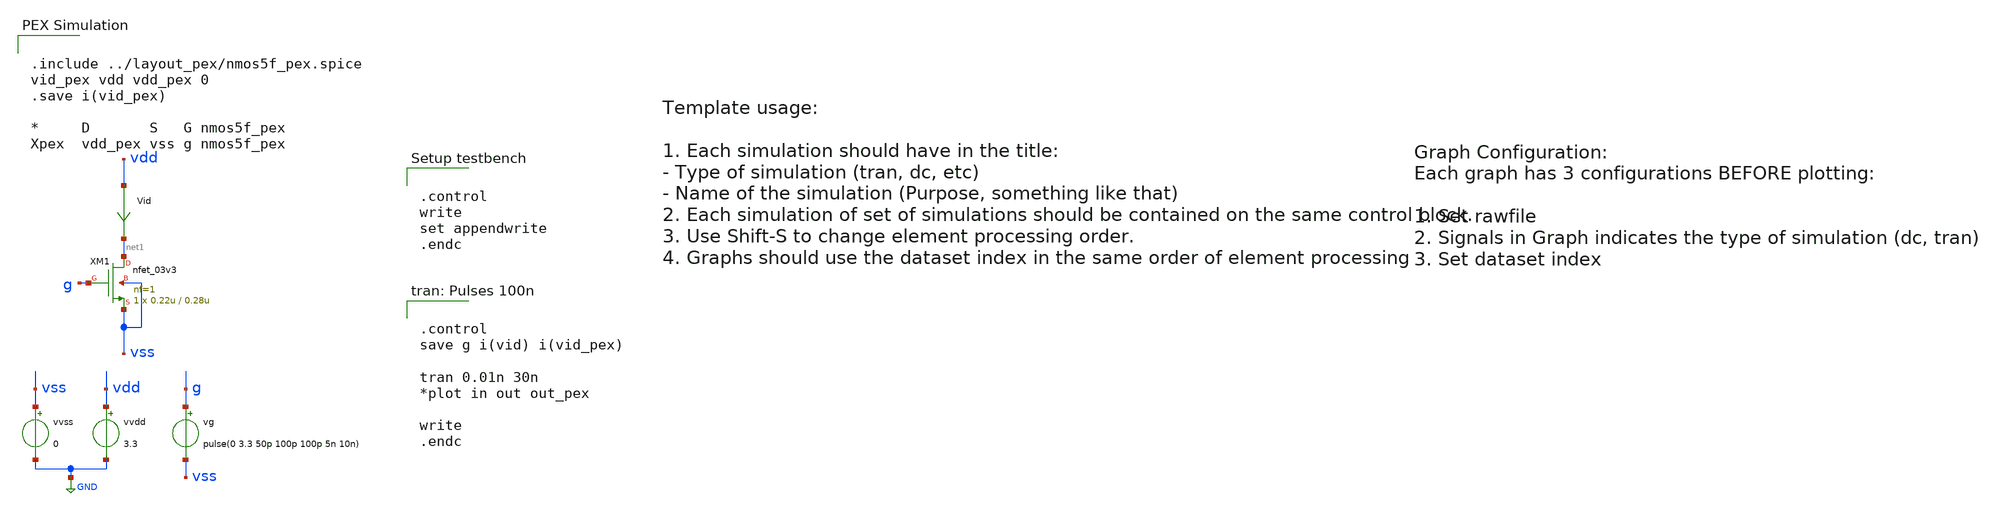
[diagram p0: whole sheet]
** sch_path: samples/gf180mcu/nmos5f/test/nmos5f.sch

.include $env(PDK_ROOT)/$env(PDK)/libs.tech/ngspice/design.ngspice
.lib $env(PDK_ROOT)/$env(PDK)/libs.tech/ngspice/sm141064.ngspice typical
.lib $env(PDK_ROOT)/$env(PDK)/libs.tech/ngspice/sm141064.ngspice mimcap_statistical
.lib $env(PDK_ROOT)/$env(PDK)/libs.tech/ngspice/sm141064.ngspice cap_mim
.lib $env(PDK_ROOT)/$env(PDK)/libs.tech/ngspice/sm141064.ngspice res_typical
.lib $env(PDK_ROOT)/$env(PDK)/libs.tech/ngspice/sm141064.ngspice bjt_typical
.lib $env(PDK_ROOT)/$env(PDK)/libs.tech/ngspice/sm141064.ngspice moscap_typical


.control
write
set appendwrite
.endc


**.subckt nmos5f
vvdd vdd GND 3.3
vg g vss pulse(0 3.3 50p 100p 100p 5n 10n)
vvss vss GND 0
XM1 net1 g vss vss nfet_03v3 L=0.28u W=0.22u nf=1 ad='int((nf+1)/2) * W/nf * 0.18u' as='int((nf+2)/2) * W/nf * 0.18u'
+ pd='2*int((nf+1)/2) * (W/nf + 0.18u)' ps='2*int((nf+2)/2) * (W/nf + 0.18u)' nrd='0.18u / W' nrs='0.18u / W'
+ sa=0 sb=0 sd=0 m=1
Vid vdd net1 0
.save i(vid)
**** begin user architecture code


.control
save g i(vid) i(vid_pex)

tran 0.01n 30n
*plot in out out_pex

write
.endc




.include ../layout_pex/nmos5f_pex.spice
vid_pex vdd vdd_pex 0
.save i(vid_pex)

*     D       S   G nmos5f_pex
Xpex  vdd_pex vss g nmos5f_pex




.control
save all

*compose voltage start=1.8 stop=3.3 step=0.5
*foreach volt $&voltage
*alterparam VGS=$volt
reset
dc vg 0 3.3 0.01
write

.endc


**** end user architecture code
**.ends
.GLOBAL GND
.end
